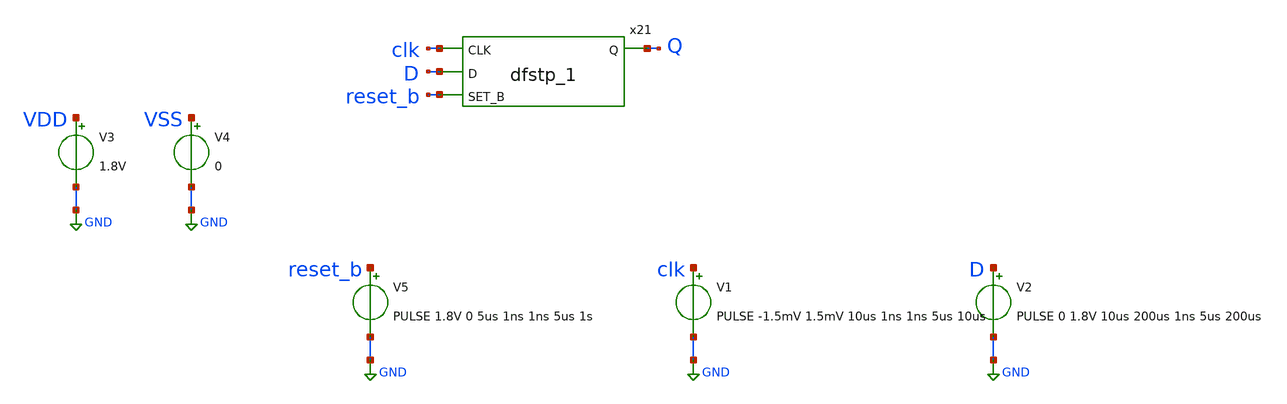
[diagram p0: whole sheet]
** sch_path: xschem/tests/dummy_tests/dummy_dff_set_test.sch
**.subckt dummy_dff_set_test
V3 VDD GND 1.8V
V4 VSS GND 0
x21 clk D reset_b VSS VSS VDD VDD Q sky130_fd_sc_hd__dfstp_1
V5 reset_b GND PULSE 1.8V 0 5us 1ns 1ns 5us 1s
V1 clk GND PULSE -1.5mV 1.5mV 10us 1ns 1ns 5us 10us
V2 D GND PULSE 0 1.8V 10us 200us 1ns 5us 200us
**** begin user architecture code
 .lib $::SKYWATER_MODELS/sky130.lib.spice tt
.include $::SKYWATER_STDCELLS/sky130_fd_sc_hd.spice


.options acct list
.temp 25
*vvcc VDD 0 dc 1.8
*vvss VSS 0 0
.control
tran 0.1u 200u
*plot RST_PLS clk+2 Pulse+4
plot clk reset_b-2 D+2 Q+4
write dummy_dff_set_test.raw
.endc


**** end user architecture code
**.ends
.GLOBAL GND
.end
